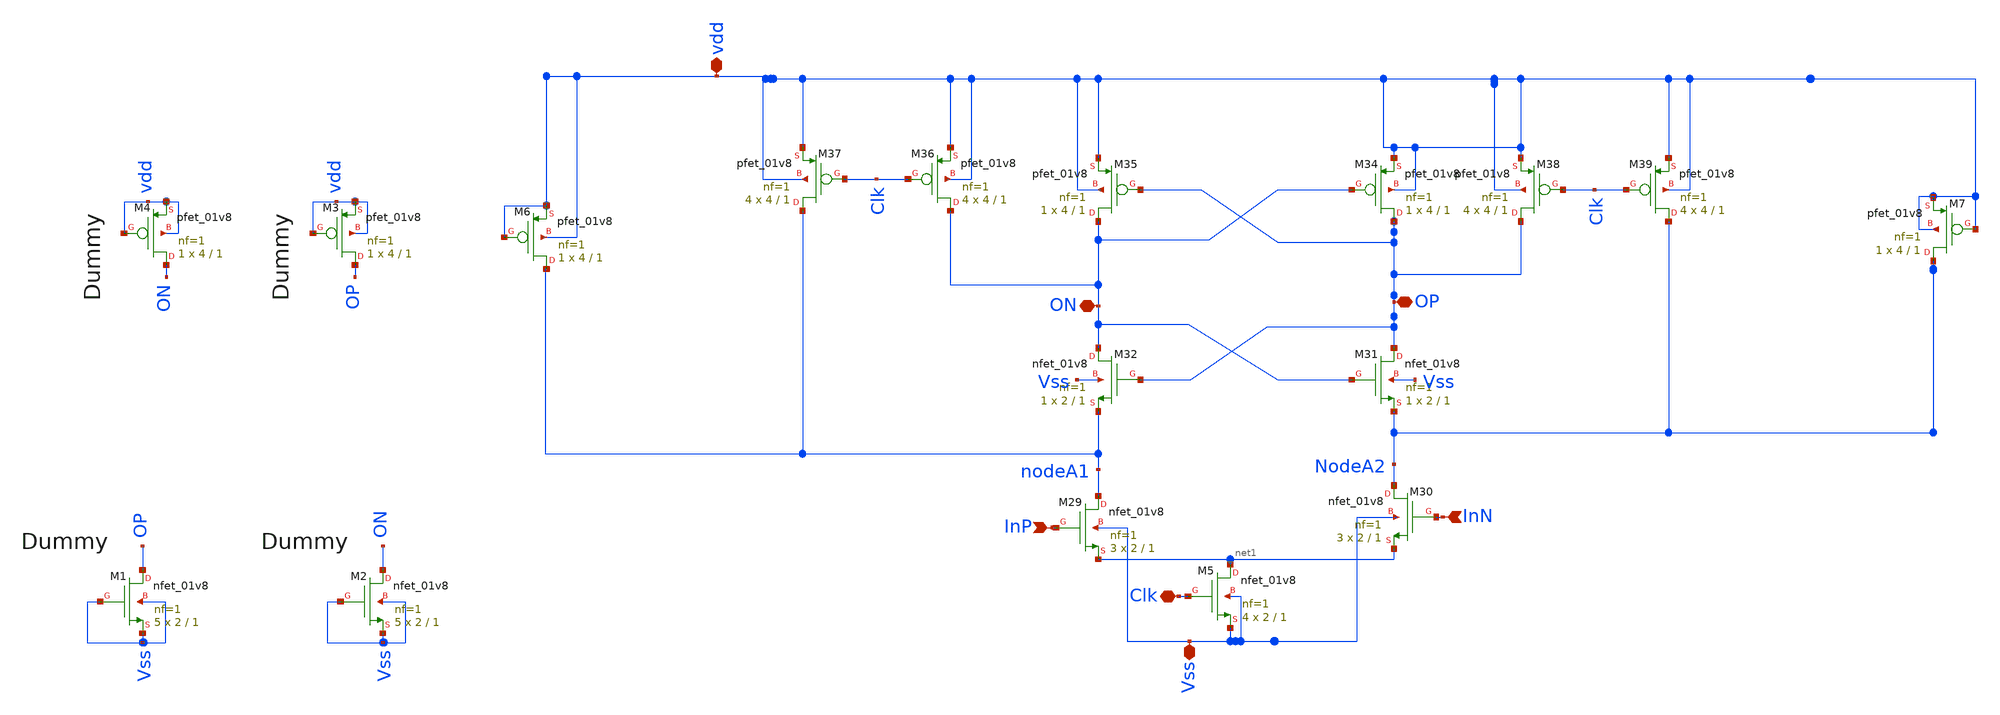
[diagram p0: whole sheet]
** sch_path: xschem/quantizer_c.sch
**.subckt quantizer_c Vss vdd Clk InP InN ON OP
*.iopin Vss
*.iopin vdd
*.iopin Clk
*.ipin InP
*.ipin InN
*.iopin ON
*.iopin OP
XM29 nodeA1 InP net1 Vss sky130_fd_pr__nfet_01v8 L=1 W=2 nf=1 ad='int((nf+1)/2) * W/nf * 0.29' as='int((nf+2)/2) * W/nf * 0.29'
+ pd='2*int((nf+1)/2) * (W/nf + 0.29)' ps='2*int((nf+2)/2) * (W/nf + 0.29)' nrd='0.29 / W' nrs='0.29 / W'
+ sa=0 sb=0 sd=0 mult=3 m=3
XM30 NodeA2 InN net1 Vss sky130_fd_pr__nfet_01v8 L=1 W=2 nf=1 ad='int((nf+1)/2) * W/nf * 0.29' as='int((nf+2)/2) * W/nf * 0.29'
+ pd='2*int((nf+1)/2) * (W/nf + 0.29)' ps='2*int((nf+2)/2) * (W/nf + 0.29)' nrd='0.29 / W' nrs='0.29 / W'
+ sa=0 sb=0 sd=0 mult=3 m=3
XM31 OP ON NodeA2 Vss sky130_fd_pr__nfet_01v8 L=1 W=2 nf=1 ad='int((nf+1)/2) * W/nf * 0.29' as='int((nf+2)/2) * W/nf * 0.29'
+ pd='2*int((nf+1)/2) * (W/nf + 0.29)' ps='2*int((nf+2)/2) * (W/nf + 0.29)' nrd='0.29 / W' nrs='0.29 / W'
+ sa=0 sb=0 sd=0 mult=1 m=1
XM32 ON OP nodeA1 Vss sky130_fd_pr__nfet_01v8 L=1 W=2 nf=1 ad='int((nf+1)/2) * W/nf * 0.29' as='int((nf+2)/2) * W/nf * 0.29'
+ pd='2*int((nf+1)/2) * (W/nf + 0.29)' ps='2*int((nf+2)/2) * (W/nf + 0.29)' nrd='0.29 / W' nrs='0.29 / W'
+ sa=0 sb=0 sd=0 mult=1 m=1
XM34 OP ON vdd vdd sky130_fd_pr__pfet_01v8 L=1 W=4 nf=1 ad='int((nf+1)/2) * W/nf * 0.29' as='int((nf+2)/2) * W/nf * 0.29'
+ pd='2*int((nf+1)/2) * (W/nf + 0.29)' ps='2*int((nf+2)/2) * (W/nf + 0.29)' nrd='0.29 / W' nrs='0.29 / W'
+ sa=0 sb=0 sd=0 mult=1 m=1
XM35 ON OP vdd vdd sky130_fd_pr__pfet_01v8 L=1 W=4 nf=1 ad='int((nf+1)/2) * W/nf * 0.29' as='int((nf+2)/2) * W/nf * 0.29'
+ pd='2*int((nf+1)/2) * (W/nf + 0.29)' ps='2*int((nf+2)/2) * (W/nf + 0.29)' nrd='0.29 / W' nrs='0.29 / W'
+ sa=0 sb=0 sd=0 mult=1 m=1
XM36 ON Clk vdd vdd sky130_fd_pr__pfet_01v8 L=1 W=4 nf=1 ad='int((nf+1)/2) * W/nf * 0.29' as='int((nf+2)/2) * W/nf * 0.29'
+ pd='2*int((nf+1)/2) * (W/nf + 0.29)' ps='2*int((nf+2)/2) * (W/nf + 0.29)' nrd='0.29 / W' nrs='0.29 / W'
+ sa=0 sb=0 sd=0 mult=4 m=4
XM37 nodeA1 Clk vdd vdd sky130_fd_pr__pfet_01v8 L=1 W=4 nf=1 ad='int((nf+1)/2) * W/nf * 0.29' as='int((nf+2)/2) * W/nf * 0.29'
+ pd='2*int((nf+1)/2) * (W/nf + 0.29)' ps='2*int((nf+2)/2) * (W/nf + 0.29)' nrd='0.29 / W' nrs='0.29 / W'
+ sa=0 sb=0 sd=0 mult=4 m=4
XM38 OP Clk vdd vdd sky130_fd_pr__pfet_01v8 L=1 W=4 nf=1 ad='int((nf+1)/2) * W/nf * 0.29' as='int((nf+2)/2) * W/nf * 0.29'
+ pd='2*int((nf+1)/2) * (W/nf + 0.29)' ps='2*int((nf+2)/2) * (W/nf + 0.29)' nrd='0.29 / W' nrs='0.29 / W'
+ sa=0 sb=0 sd=0 mult=4 m=4
XM39 NodeA2 Clk vdd vdd sky130_fd_pr__pfet_01v8 L=1 W=4 nf=1 ad='int((nf+1)/2) * W/nf * 0.29' as='int((nf+2)/2) * W/nf * 0.29'
+ pd='2*int((nf+1)/2) * (W/nf + 0.29)' ps='2*int((nf+2)/2) * (W/nf + 0.29)' nrd='0.29 / W' nrs='0.29 / W'
+ sa=0 sb=0 sd=0 mult=4 m=4
XM2 ON Vss Vss Vss sky130_fd_pr__nfet_01v8 L=1 W=2 nf=1 ad='int((nf+1)/2) * W/nf * 0.29' as='int((nf+2)/2) * W/nf * 0.29'
+ pd='2*int((nf+1)/2) * (W/nf + 0.29)' ps='2*int((nf+2)/2) * (W/nf + 0.29)' nrd='0.29 / W' nrs='0.29 / W'
+ sa=0 sb=0 sd=0 mult=5 m=5
XM3 OP vdd vdd vdd sky130_fd_pr__pfet_01v8 L=1 W=4 nf=1 ad='int((nf+1)/2) * W/nf * 0.29' as='int((nf+2)/2) * W/nf * 0.29'
+ pd='2*int((nf+1)/2) * (W/nf + 0.29)' ps='2*int((nf+2)/2) * (W/nf + 0.29)' nrd='0.29 / W' nrs='0.29 / W'
+ sa=0 sb=0 sd=0 mult=1 m=1
XM5 net1 Clk Vss Vss sky130_fd_pr__nfet_01v8 L=1 W=2 nf=1 ad='int((nf+1)/2) * W/nf * 0.29' as='int((nf+2)/2) * W/nf * 0.29'
+ pd='2*int((nf+1)/2) * (W/nf + 0.29)' ps='2*int((nf+2)/2) * (W/nf + 0.29)' nrd='0.29 / W' nrs='0.29 / W'
+ sa=0 sb=0 sd=0 mult=4 m=4
XM6 nodeA1 vdd vdd vdd sky130_fd_pr__pfet_01v8 L=1 W=4 nf=1 ad='int((nf+1)/2) * W/nf * 0.29' as='int((nf+2)/2) * W/nf * 0.29'
+ pd='2*int((nf+1)/2) * (W/nf + 0.29)' ps='2*int((nf+2)/2) * (W/nf + 0.29)' nrd='0.29 / W' nrs='0.29 / W'
+ sa=0 sb=0 sd=0 mult=1 m=1
XM7 NodeA2 vdd vdd vdd sky130_fd_pr__pfet_01v8 L=1 W=4 nf=1 ad='int((nf+1)/2) * W/nf * 0.29' as='int((nf+2)/2) * W/nf * 0.29'
+ pd='2*int((nf+1)/2) * (W/nf + 0.29)' ps='2*int((nf+2)/2) * (W/nf + 0.29)' nrd='0.29 / W' nrs='0.29 / W'
+ sa=0 sb=0 sd=0 mult=1 m=1
XM1 OP Vss Vss Vss sky130_fd_pr__nfet_01v8 L=1 W=2 nf=1 ad='int((nf+1)/2) * W/nf * 0.29' as='int((nf+2)/2) * W/nf * 0.29'
+ pd='2*int((nf+1)/2) * (W/nf + 0.29)' ps='2*int((nf+2)/2) * (W/nf + 0.29)' nrd='0.29 / W' nrs='0.29 / W'
+ sa=0 sb=0 sd=0 mult=5 m=5
XM4 ON vdd vdd vdd sky130_fd_pr__pfet_01v8 L=1 W=4 nf=1 ad='int((nf+1)/2) * W/nf * 0.29' as='int((nf+2)/2) * W/nf * 0.29'
+ pd='2*int((nf+1)/2) * (W/nf + 0.29)' ps='2*int((nf+2)/2) * (W/nf + 0.29)' nrd='0.29 / W' nrs='0.29 / W'
+ sa=0 sb=0 sd=0 mult=1 m=1
**.ends
.end
